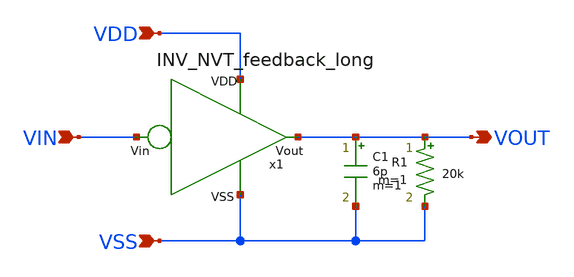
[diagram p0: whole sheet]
** sch_path: design/THESIS_EXP_RO_INVERTER_SKY130A/TB_Cin_NVT_L.sch
**.subckt TB_Cin_NVT_L VOUT VIN VSS VDD
*.opin VOUT
*.ipin VIN
*.ipin VSS
*.ipin VDD
C1 VOUT VSS 6p m=1
R1 VOUT VSS 20k m=1
x1 VDD VSS VOUT VIN INV_NVT_feedback_long
**.ends

* expanding   symbol:  THESIS_EXP_RO_INVERTER_SKY130A/INV_NVT_feedback_long.sym # of pins=4
** sym_path: design/THESIS_EXP_RO_INVERTER_SKY130A/INV_NVT_feedback_long.sym
** sch_path: design/THESIS_EXP_RO_INVERTER_SKY130A/INV_NVT_feedback_long.sch
.subckt INV_NVT_feedback_long VDD VSS Vout Vin
*.ipin VSS
*.ipin Vin
*.opin Vout
*.ipin VDD
XM1 Vout Vin VDD VDD sky130_fd_pr__pfet_01v8_lvt L=0.35 W=7 nf=1 ad='int((nf+1)/2) * W/nf * 0.29' as='int((nf+2)/2) * W/nf * 0.29'
+ pd='2*int((nf+1)/2) * (W/nf + 0.29)' ps='2*int((nf+2)/2) * (W/nf + 0.29)' nrd='0.29 / W' nrs='0.29 / W'
+ sa=0 sb=0 sd=0 mult=m_alpha m=m_alpha
XM2 Vout Vin vn VSS sky130_fd_pr__nfet_03v3_nvt L=0.8 W=0.42 nf=1 ad='int((nf+1)/2) * W/nf * 0.29' as='int((nf+2)/2) * W/nf * 0.29'
+ pd='2*int((nf+1)/2) * (W/nf + 0.29)' ps='2*int((nf+2)/2) * (W/nf + 0.29)' nrd='0.29 / W' nrs='0.29 / W'
+ sa=0 sb=0 sd=0 mult=m_beta m=m_beta
XM3 vn Vin VSS VSS sky130_fd_pr__nfet_03v3_nvt L=0.8 W=0.42 nf=1 ad='int((nf+1)/2) * W/nf * 0.29' as='int((nf+2)/2) * W/nf * 0.29'
+ pd='2*int((nf+1)/2) * (W/nf + 0.29)' ps='2*int((nf+2)/2) * (W/nf + 0.29)' nrd='0.29 / W' nrs='0.29 / W'
+ sa=0 sb=0 sd=0 mult=m_I0 m=m_I0
XM4 VDD Vout vn VSS sky130_fd_pr__nfet_03v3_nvt L=0.8 W=0.42 nf=1 ad='int((nf+1)/2) * W/nf * 0.29' as='int((nf+2)/2) * W/nf * 0.29'
+ pd='2*int((nf+1)/2) * (W/nf + 0.29)' ps='2*int((nf+2)/2) * (W/nf + 0.29)' nrd='0.29 / W' nrs='0.29 / W'
+ sa=0 sb=0 sd=0 mult=m_gamma m=m_gamma
.ends

.end
